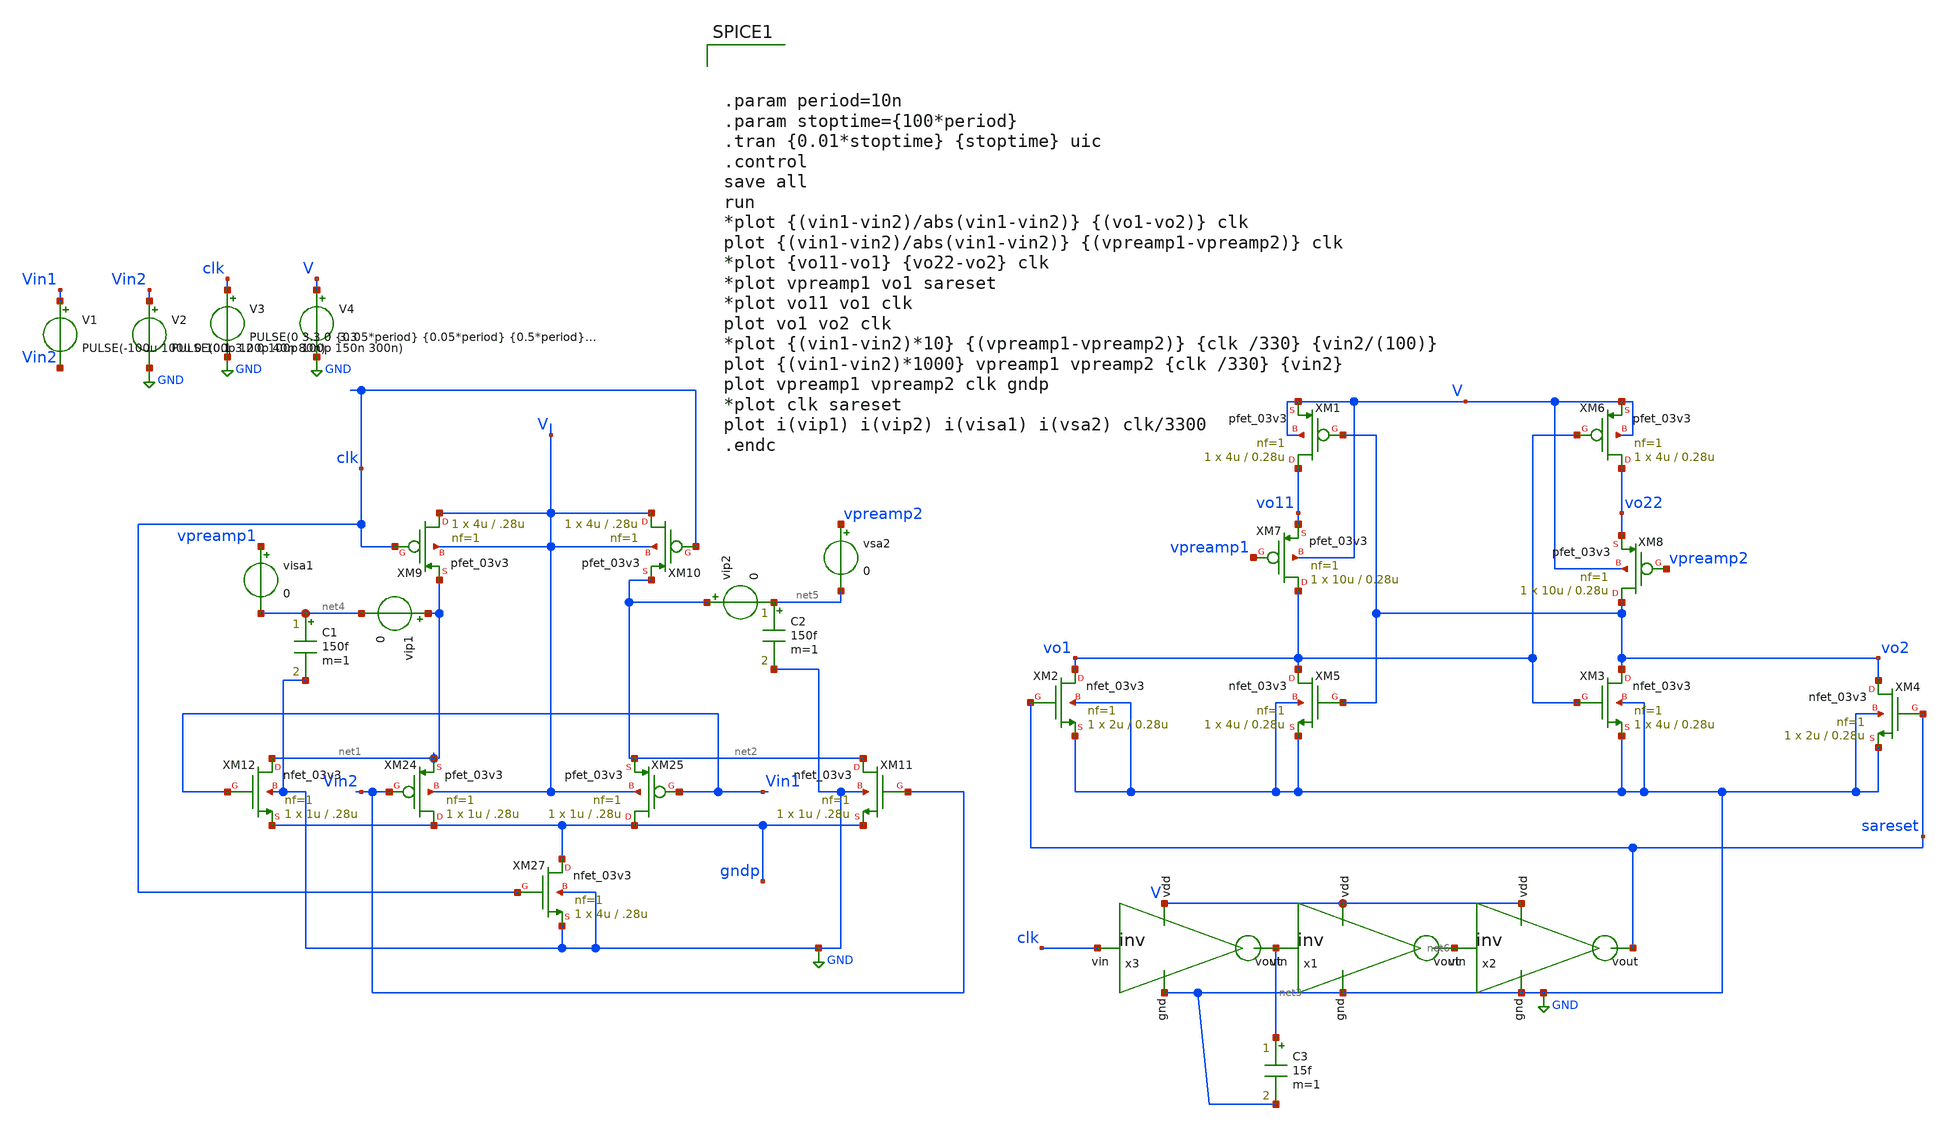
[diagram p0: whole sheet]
** sch_path: xschem/test/comp_full_tb/comp_random_tb.sch
**.subckt comp_random_tb
V3 clk GND PULSE(0 3.3 0 {0.05*period} {0.05*period} {0.5*period} {1*period})
V4 V GND 3.3
XM1 vo11 vo2 V V pfet_03v3 L=0.28u W=4u nf=1 ad='int((nf+1)/2) * W/nf * 0.18u' as='int((nf+2)/2) * W/nf * 0.18u'
+ pd='2*int((nf+1)/2) * (W/nf + 0.18u)' ps='2*int((nf+2)/2) * (W/nf + 0.18u)' nrd='0.18u / W' nrs='0.18u / W'
+ sa=0 sb=0 sd=0 m=1
XM2 vo1 sareset GND GND nfet_03v3 L=0.28u W=2u nf=1 ad='int((nf+1)/2) * W/nf * 0.18u' as='int((nf+2)/2) * W/nf * 0.18u'
+ pd='2*int((nf+1)/2) * (W/nf + 0.18u)' ps='2*int((nf+2)/2) * (W/nf + 0.18u)' nrd='0.18u / W' nrs='0.18u / W'
+ sa=0 sb=0 sd=0 m=1
XM3 vo2 vo1 GND GND nfet_03v3 L=0.28u W=4u nf=1 ad='int((nf+1)/2) * W/nf * 0.18u' as='int((nf+2)/2) * W/nf * 0.18u'
+ pd='2*int((nf+1)/2) * (W/nf + 0.18u)' ps='2*int((nf+2)/2) * (W/nf + 0.18u)' nrd='0.18u / W' nrs='0.18u / W'
+ sa=0 sb=0 sd=0 m=1
XM4 vo2 sareset GND GND nfet_03v3 L=0.28u W=2u nf=1 ad='int((nf+1)/2) * W/nf * 0.18u' as='int((nf+2)/2) * W/nf * 0.18u'
+ pd='2*int((nf+1)/2) * (W/nf + 0.18u)' ps='2*int((nf+2)/2) * (W/nf + 0.18u)' nrd='0.18u / W' nrs='0.18u / W'
+ sa=0 sb=0 sd=0 m=1
XM5 vo1 vo2 GND GND nfet_03v3 L=0.28u W=4u nf=1 ad='int((nf+1)/2) * W/nf * 0.18u' as='int((nf+2)/2) * W/nf * 0.18u'
+ pd='2*int((nf+1)/2) * (W/nf + 0.18u)' ps='2*int((nf+2)/2) * (W/nf + 0.18u)' nrd='0.18u / W' nrs='0.18u / W'
+ sa=0 sb=0 sd=0 m=1
XM6 vo22 vo1 V V pfet_03v3 L=0.28u W=4u nf=1 ad='int((nf+1)/2) * W/nf * 0.18u' as='int((nf+2)/2) * W/nf * 0.18u'
+ pd='2*int((nf+1)/2) * (W/nf + 0.18u)' ps='2*int((nf+2)/2) * (W/nf + 0.18u)' nrd='0.18u / W' nrs='0.18u / W'
+ sa=0 sb=0 sd=0 m=1
XM7 vo1 vpreamp1 vo11 V pfet_03v3 L=0.28u W=10u nf=1 ad='int((nf+1)/2) * W/nf * 0.18u' as='int((nf+2)/2) * W/nf * 0.18u'
+ pd='2*int((nf+1)/2) * (W/nf + 0.18u)' ps='2*int((nf+2)/2) * (W/nf + 0.18u)' nrd='0.18u / W' nrs='0.18u / W'
+ sa=0 sb=0 sd=0 m=1
XM8 vo2 vpreamp2 vo22 V pfet_03v3 L=0.28u W=10u nf=1 ad='int((nf+1)/2) * W/nf * 0.18u' as='int((nf+2)/2) * W/nf * 0.18u'
+ pd='2*int((nf+1)/2) * (W/nf + 0.18u)' ps='2*int((nf+2)/2) * (W/nf + 0.18u)' nrd='0.18u / W' nrs='0.18u / W'
+ sa=0 sb=0 sd=0 m=1
x3 V GND net3 clk inv cl=0.28u wp=0.44u wn=0.22u wx=.22u mx=1
XM27 gndp clk GND GND nfet_03v3 L=.28u W=4u nf=1 ad='int((nf+1)/2) * W/nf * 0.18u' as='int((nf+2)/2) * W/nf * 0.18u'
+ pd='2*int((nf+1)/2) * (W/nf + 0.18u)' ps='2*int((nf+2)/2) * (W/nf + 0.18u)' nrd='0.18u / W' nrs='0.18u / W'
+ sa=0 sb=0 sd=0 m=1
XM24 gndp Vin2 net1 V pfet_03v3 L=.28u W=1u nf=1 ad='int((nf+1)/2) * W/nf * 0.18u' as='int((nf+2)/2) * W/nf * 0.18u'
+ pd='2*int((nf+1)/2) * (W/nf + 0.18u)' ps='2*int((nf+2)/2) * (W/nf + 0.18u)' nrd='0.18u / W' nrs='0.18u / W'
+ sa=0 sb=0 sd=0 m=1
XM25 gndp Vin1 net2 V pfet_03v3 L=.28u W=1u nf=1 ad='int((nf+1)/2) * W/nf * 0.18u' as='int((nf+2)/2) * W/nf * 0.18u'
+ pd='2*int((nf+1)/2) * (W/nf + 0.18u)' ps='2*int((nf+2)/2) * (W/nf + 0.18u)' nrd='0.18u / W' nrs='0.18u / W'
+ sa=0 sb=0 sd=0 m=1
XM9 V clk net1 V pfet_03v3 L=.28u W=4u nf=1 ad='int((nf+1)/2) * W/nf * 0.18u' as='int((nf+2)/2) * W/nf * 0.18u'
+ pd='2*int((nf+1)/2) * (W/nf + 0.18u)' ps='2*int((nf+2)/2) * (W/nf + 0.18u)' nrd='0.18u / W' nrs='0.18u / W'
+ sa=0 sb=0 sd=0 m=1
XM10 V clk net2 V pfet_03v3 L=.28u W=4u nf=1 ad='int((nf+1)/2) * W/nf * 0.18u' as='int((nf+2)/2) * W/nf * 0.18u'
+ pd='2*int((nf+1)/2) * (W/nf + 0.18u)' ps='2*int((nf+2)/2) * (W/nf + 0.18u)' nrd='0.18u / W' nrs='0.18u / W'
+ sa=0 sb=0 sd=0 m=1
XM11 net2 Vin2 gndp GND nfet_03v3 L=.28u W=1u nf=1 ad='int((nf+1)/2) * W/nf * 0.18u' as='int((nf+2)/2) * W/nf * 0.18u'
+ pd='2*int((nf+1)/2) * (W/nf + 0.18u)' ps='2*int((nf+2)/2) * (W/nf + 0.18u)' nrd='0.18u / W' nrs='0.18u / W'
+ sa=0 sb=0 sd=0 m=1
XM12 net1 Vin1 gndp GND nfet_03v3 L=.28u W=1u nf=1 ad='int((nf+1)/2) * W/nf * 0.18u' as='int((nf+2)/2) * W/nf * 0.18u'
+ pd='2*int((nf+1)/2) * (W/nf + 0.18u)' ps='2*int((nf+2)/2) * (W/nf + 0.18u)' nrd='0.18u / W' nrs='0.18u / W'
+ sa=0 sb=0 sd=0 m=1
C1 net4 GND 150f m=1
C2 net5 GND 150f m=1
V1 Vin1 Vin2 PULSE(-100u 100u 0 100p 100p 40n 80n)
V2 Vin2 GND PULSE(0.1 3.2 0 100p 100p 150n 300n)
x1 V GND net6 net3 inv cl=0.28u wp=0.44u wn=0.22u wx=1u mx=1
x2 V GND sareset net6 inv cl=0.28u wp=0.44u wn=0.22u wx=10u mx=1
C3 net3 GND 15f m=1
vip1 net1 net4 0
visa1 vpreamp1 net4 0
vip2 net2 net5 0
vsa2 vpreamp2 net5 0
**** begin user architecture code



.param period=10n
.param stoptime={100*period}
.tran {0.01*stoptime} {stoptime} uic
.control
save all
run
*plot {(vin1-vin2)/abs(vin1-vin2)} {(vo1-vo2)} clk
plot {(vin1-vin2)/abs(vin1-vin2)} {(vpreamp1-vpreamp2)} clk
*plot {vo11-vo1} {vo22-vo2} clk
*plot vpreamp1 vo1 sareset
*plot vo11 vo1 clk
plot vo1 vo2 clk
*plot {(vin1-vin2)*10} {(vpreamp1-vpreamp2)} {clk /330} {vin2/(100)}
plot {(vin1-vin2)*1000} vpreamp1 vpreamp2 {clk /330} {vin2}
plot vpreamp1 vpreamp2 clk gndp
*plot clk sareset
plot i(vip1) i(vip2) i(visa1) i(vsa2) clk/3300
.endc


.include $env(PDK_ROOT)/$env(PDK)/libs.tech/ngspice/design.ngspice
.lib $env(PDK_ROOT)/$env(PDK)/libs.tech/ngspice/sm141064.ngspice typical

**** end user architecture code
**.ends

* expanding   symbol:  inv.sym # of pins=4
** sym_path: xschem/designs/inv.sym
** sch_path: xschem/designs/inv.sch
.subckt inv vdd gnd vout vin  cl=0.28u wp=0.44u wn=0.22u wx=0.22u mx=1
*.ipin gnd
*.ipin vdd
*.ipin vin
*.opin vout
XM1 gnd vin vout gnd nfet_03v3 L=0.28u W=Wx nf=1 ad='int((nf+1)/2) * W/nf * 0.18u' as='int((nf+2)/2) * W/nf * 0.18u'
+ pd='2*int((nf+1)/2) * (W/nf + 0.18u)' ps='2*int((nf+2)/2) * (W/nf + 0.18u)' nrd='0.18u / W' nrs='0.18u / W'
+ sa=0 sb=0 sd=0 m=1
XM2 vdd vin vout vdd pfet_03v3 L=0.28u W=Wx nf=1 ad='int((nf+1)/2) * W/nf * 0.18u' as='int((nf+2)/2) * W/nf * 0.18u'
+ pd='2*int((nf+1)/2) * (W/nf + 0.18u)' ps='2*int((nf+2)/2) * (W/nf + 0.18u)' nrd='0.18u / W' nrs='0.18u / W'
+ sa=0 sb=0 sd=0 m=1
.ends

.GLOBAL GND
.end
